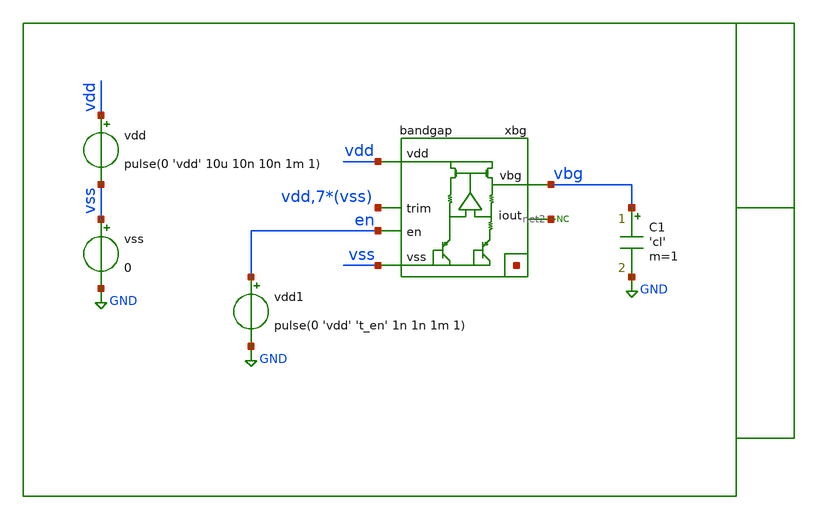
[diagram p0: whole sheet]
** sch_path: xschem/tb/bandgap_cm/bandgap/mc_bandgap_init_accuracy.sch
**.subckt mc_bandgap_init_accuracy
xbg vdd vbg vss net1[7] net1[6] net1[5] net1[4] net1[3] net1[2] net1[1] net1[0] vdd vss vss vss vss
+ vss vss vss net2 en bandgap
vss vss GND 0
C1 vbg GND 'cl' m=1
vdd vdd vss pulse(0 'vdd' 10u 10n 10n 1m 1)
* noconn #net2
vdd1 en GND pulse(0 'vdd' 't_en' 1n 1n 1m 1)
**** begin user architecture code

* Control

.param vdd = 3.3
.param cl = 500e-15

.param t_en = 20u
.csparam t_en = t_en

.temp 27
.options reltol = 1e-6


.param nseed = 2
.csparam ns = nseed

.control

alterparam sw_stat_global   = 1
alterparam sw_stat_mismatch = 1
reset

setseed $&ns

save all
tran 1u 200u

meas tran vbg_ss find v(vbg) at=199e-6

print vbg_ss

*set wr_singlescale
*set wr_vecnames
*wrdata data.csv vbg

.endc
.end


 * Model Corners

.include $::CORNERS/ngspice/tt.spice
*.include $::CORNERS/ngspice/ff.spice
*.include $::CORNERS/ngspice/ss.spice
*.include $::CORNERS/ngspice/sf.spice
*.include $::CORNERS/ngspice/fs.spice

**** end user architecture code
**.ends
.GLOBAL GND
.end
